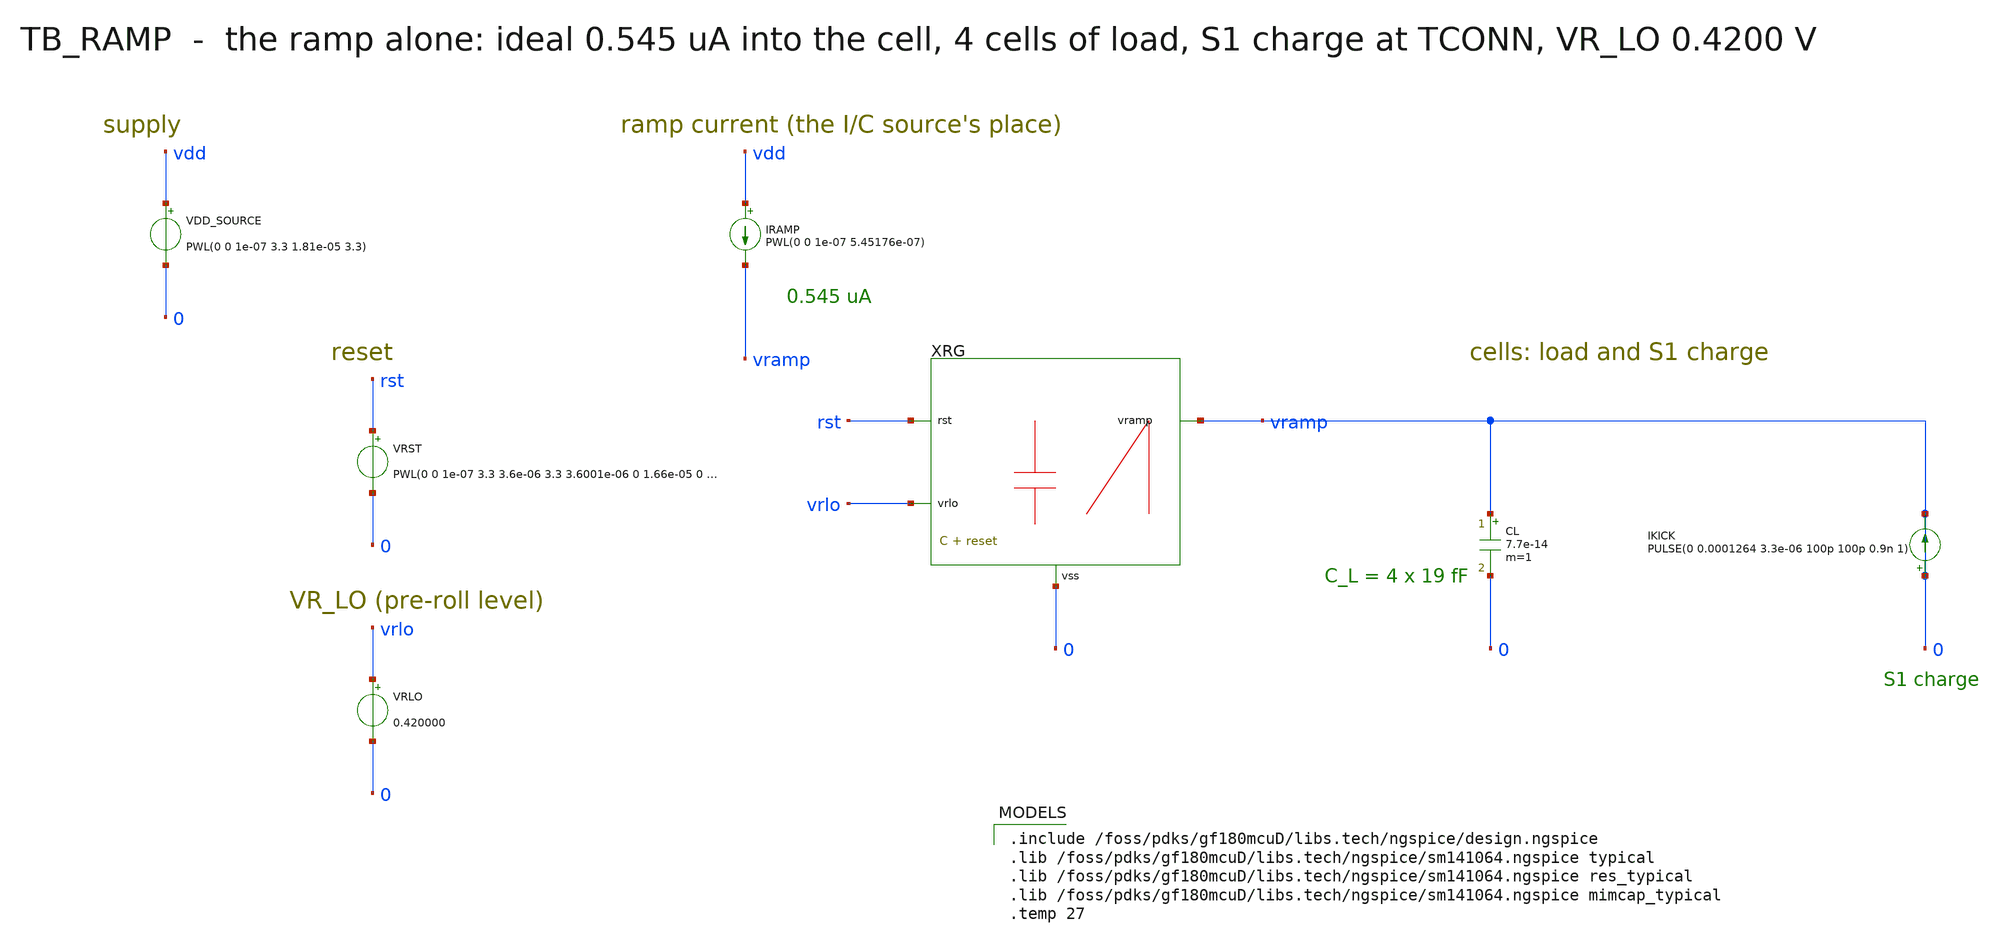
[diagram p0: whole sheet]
** sch_path: mixed_signal/ramp_simple/tb_ramp.sch
**.subckt tb_ramp
VDD_SOURCE vdd 0 PWL(0 0 1e-07 3.3 1.81e-05 3.3)
IRAMP vdd vramp PWL(0 0 1e-07 5.45176e-07)
VRST rst 0 PWL(0 0 1e-07 3.3 3.6e-06 3.3 3.6001e-06 0 1.66e-05 0 1.66001e-05 3.3)
VRLO vrlo 0 0.420000
XRG vramp rst vrlo 0 ramp_simple
CL vramp 0 7.7e-14 m=1
IKICK vramp vramp PULSE(0 0.0001264 3.3e-06 100p 100p 0.9n 1)
**** begin user architecture code

.include /foss/pdks/gf180mcuD/libs.tech/ngspice/design.ngspice
.lib /foss/pdks/gf180mcuD/libs.tech/ngspice/sm141064.ngspice typical
.lib /foss/pdks/gf180mcuD/libs.tech/ngspice/sm141064.ngspice res_typical
.lib /foss/pdks/gf180mcuD/libs.tech/ngspice/sm141064.ngspice mimcap_typical
.temp 27

**** end user architecture code
**.ends
.end
